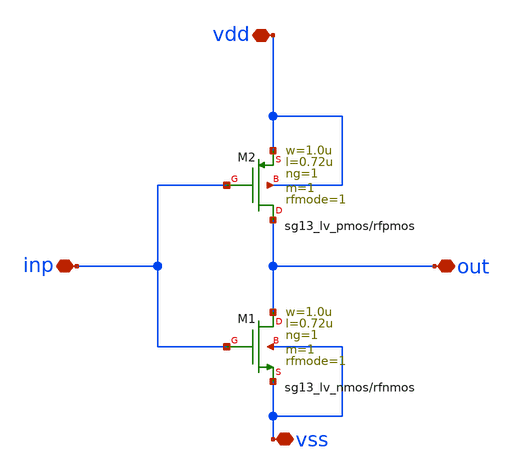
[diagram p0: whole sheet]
** sch_path: LNA7096-main/schematic/xschem/01_lna/inv.sch
**.subckt inv vss out inp vdd
*.iopin vss
*.iopin out
*.iopin inp
*.iopin vdd
XM1 out inp vss vss sg13_lv_nmos w=1.0u l=0.72u ng=1 m=1 rfmode=1 mm_ok=1
XM2 out inp vdd vdd sg13_lv_pmos w=1.0u l=0.72u ng=1 m=1 rfmode=1 mm_ok=1
**.ends
.end
